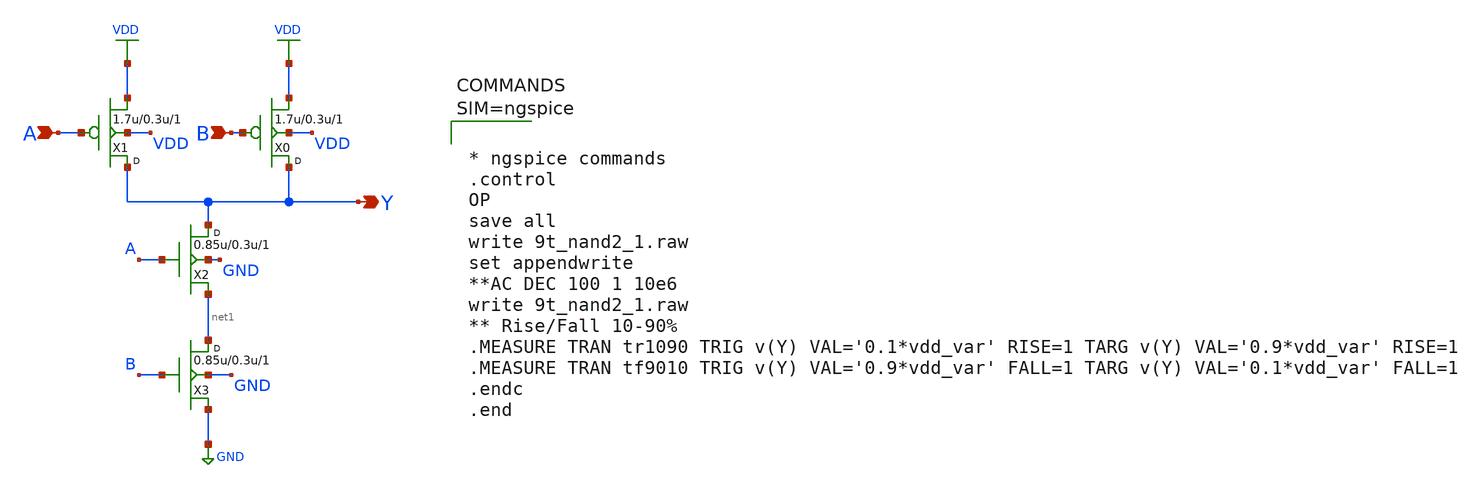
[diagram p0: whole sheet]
** sch_path: xschem/9t_nand2_1.sch
**.subckt 9t_nand2_1 A B Y
*.ipin A
*.ipin B
*.opin Y
X1 Y A VDD VDD pfet_03p3 w=1.7u l=0.3u m=1
X0 Y B VDD VDD pfet_03p3 w=1.7u l=0.3u m=1
X2 Y A net1 GND nfet_03p3 w=0.85u l=0.3u m=1
X3 net1 B GND GND nfet_03p3 w=0.85u l=0.3u m=1
**** begin user architecture code



* ngspice commands
.control
OP
save all
write 9t_nand2_1.raw
set appendwrite
**AC DEC 100 1 10e6
write 9t_nand2_1.raw
** Rise/Fall 10-90%
.MEASURE TRAN tr1090 TRIG v(Y) VAL='0.1*vdd_var' RISE=1 TARG v(Y) VAL='0.9*vdd_var' RISE=1
.MEASURE TRAN tf9010 TRIG v(Y) VAL='0.9*vdd_var' FALL=1 TARG v(Y) VAL='0.1*vdd_var' FALL=1
.endc
.end



**** end user architecture code
**.ends
.GLOBAL VDD
.GLOBAL GND
.end
